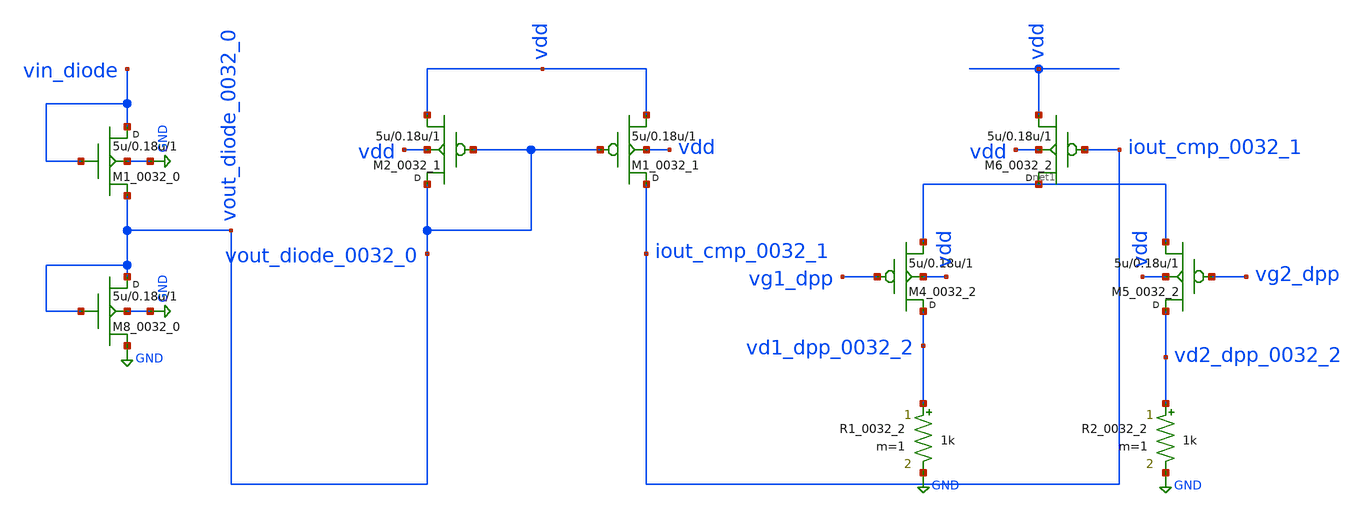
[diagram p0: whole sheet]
** sch_path: synthetic/generated/0032_generated.sch
**.subckt 0032_generated
M8_0032_0 vout_diode_0032_0 vout_diode_0032_0 GND GND nmos w=5u l=0.18u m=1
M1_0032_0 vin_diode vin_diode vout_diode_0032_0 GND nmos w=5u l=0.18u m=1
M1_0032_1 iout_cmp_0032_1 vout_diode_0032_0 vdd vdd pmos w=5u l=0.18u m=1
M2_0032_1 vout_diode_0032_0 vout_diode_0032_0 vdd vdd pmos w=5u l=0.18u m=1
M4_0032_2 vd1_dpp_0032_2 vg1_dpp net1 vdd pmos w=5u l=0.18u m=1
M5_0032_2 vd2_dpp_0032_2 vg2_dpp net1 vdd pmos w=5u l=0.18u m=1
M6_0032_2 net1 iout_cmp_0032_1 vdd vdd pmos w=5u l=0.18u m=1
R1_0032_2 vd1_dpp_0032_2 GND 1k m=1
R2_0032_2 vd2_dpp_0032_2 GND 1k m=1
**.ends
.GLOBAL GND
.end
